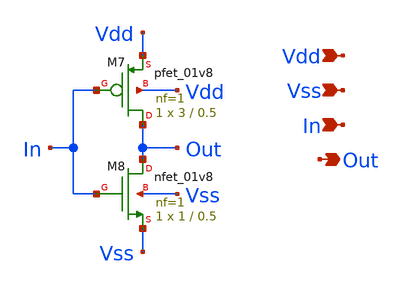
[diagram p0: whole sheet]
** sch_path: temp_sensor_sky130nm/design/TEMP_SENSOR_SKY130NM/INV.sch
**.subckt INV Vdd Vss In Out
*.ipin Vdd
*.ipin Vss
*.ipin In
*.opin Out
XM7 Out In Vdd Vdd sky130_fd_pr__pfet_01v8 L=0.5 W=3 nf=1 ad='int((nf+1)/2) * W/nf * 0.29' as='int((nf+2)/2) * W/nf * 0.29'
+ pd='2*int((nf+1)/2) * (W/nf + 0.29)' ps='2*int((nf+2)/2) * (W/nf + 0.29)' nrd='0.29 / W' nrs='0.29 / W'
+ sa=0 sb=0 sd=0 mult=1 m=1
XM8 Out In Vss Vss sky130_fd_pr__nfet_01v8 L=0.5 W=1 nf=1 ad='int((nf+1)/2) * W/nf * 0.29' as='int((nf+2)/2) * W/nf * 0.29'
+ pd='2*int((nf+1)/2) * (W/nf + 0.29)' ps='2*int((nf+2)/2) * (W/nf + 0.29)' nrd='0.29 / W' nrs='0.29 / W'
+ sa=0 sb=0 sd=0 mult=1 m=1
**.ends
.end
